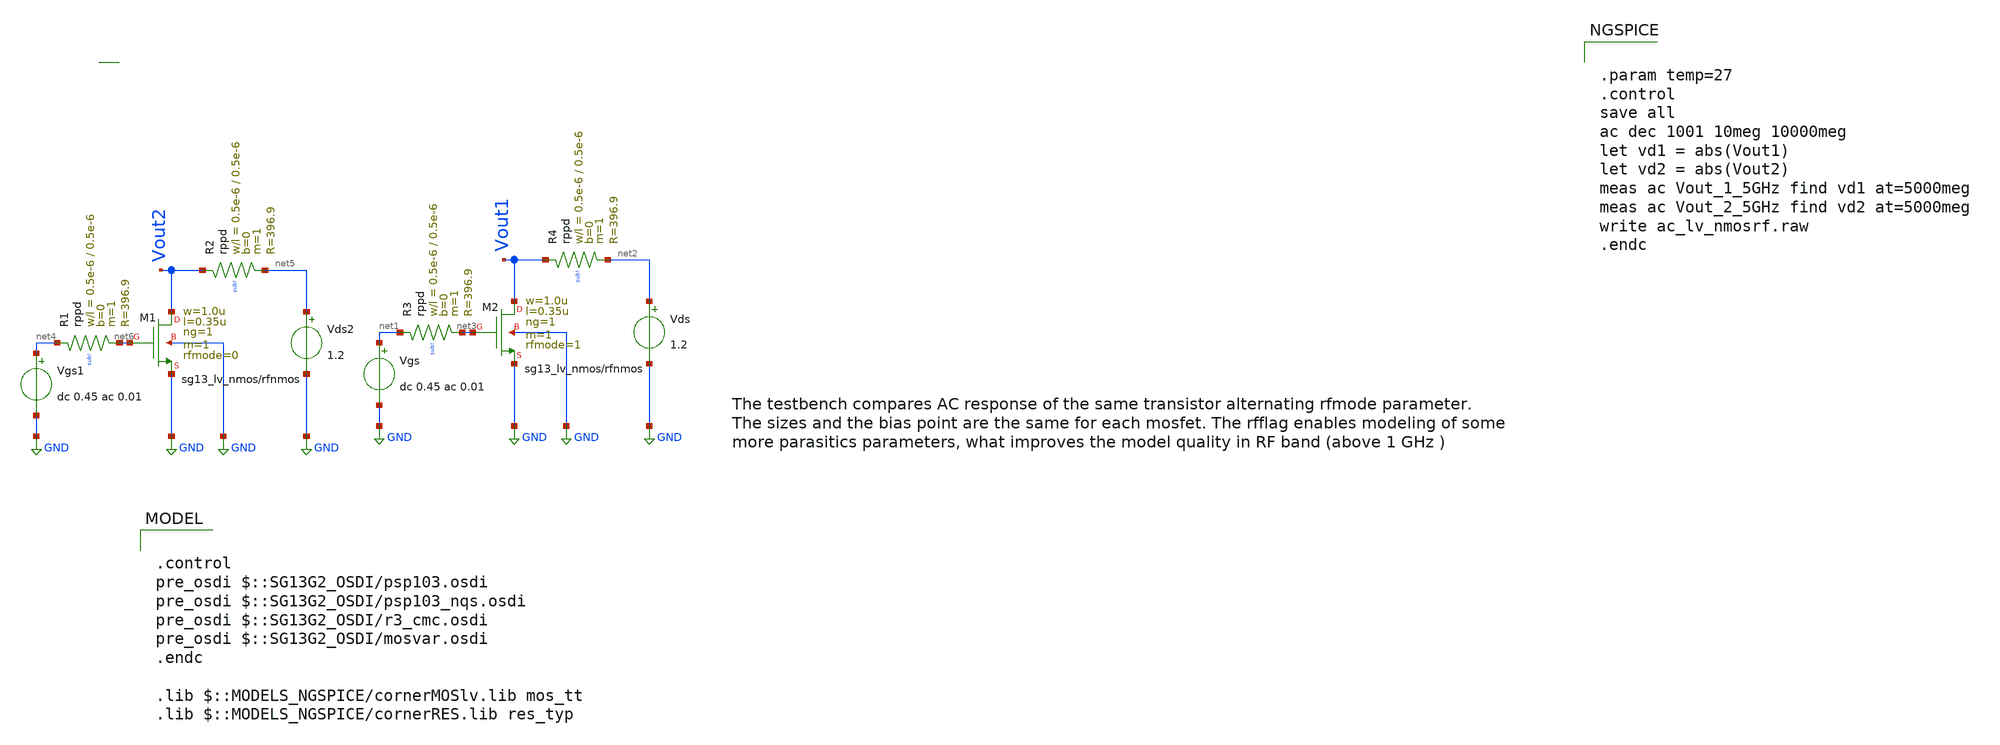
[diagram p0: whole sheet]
** sch_path: ihp-sg13g2/xschem_libs/sg13g2_tests/ac_lv_nmosrf/schematic/ac_lv_nmosrf.sch
* Copyright 2023 IHP PDK Authors
**.subckt ac_lv_nmosrf
Vgs net1 GND dc 0.45 ac 0.01
Vds net2 GND 1.2
Vgs1 net4 GND dc 0.45 ac 0.01
Vds2 net5 GND 1.2
XR1 net4 net6 sub! rppd w=0.5e-6 l=0.5e-6 m=1 b=0 mm_ok=1
XR2 Vout2 net5 sub! rppd w=0.5e-6 l=0.5e-6 m=1 b=0 mm_ok=1
XR3 net1 net3 sub! rppd w=0.5e-6 l=0.5e-6 m=1 b=0 mm_ok=1
XR4 Vout1 net2 sub! rppd w=0.5e-6 l=0.5e-6 m=1 b=0 mm_ok=1
XM1 Vout2 net6 GND GND sg13_lv_nmos w=1.0u l=0.35u ng=1 m=1 rfmode=0 mm_ok=1
XM2 Vout1 net3 GND GND sg13_lv_nmos w=1.0u l=0.35u ng=1 m=1 rfmode=1 mm_ok=1
**** begin user architecture code

.control
pre_osdi $::SG13G2_OSDI/psp103.osdi
pre_osdi $::SG13G2_OSDI/psp103_nqs.osdi
pre_osdi $::SG13G2_OSDI/r3_cmc.osdi
pre_osdi $::SG13G2_OSDI/mosvar.osdi
.endc

.lib $::MODELS_NGSPICE/cornerMOSlv.lib mos_tt
.lib $::MODELS_NGSPICE/cornerRES.lib res_typ



.param temp=27
.control
save all
ac dec 1001 10meg 10000meg
let vd1 = abs(Vout1)
let vd2 = abs(Vout2)
meas ac Vout_1_5GHz find vd1 at=5000meg
meas ac Vout_2_5GHz find vd2 at=5000meg
write ac_lv_nmosrf.raw
.endc


**** end user architecture code
**.ends
.GLOBAL GND
.end
